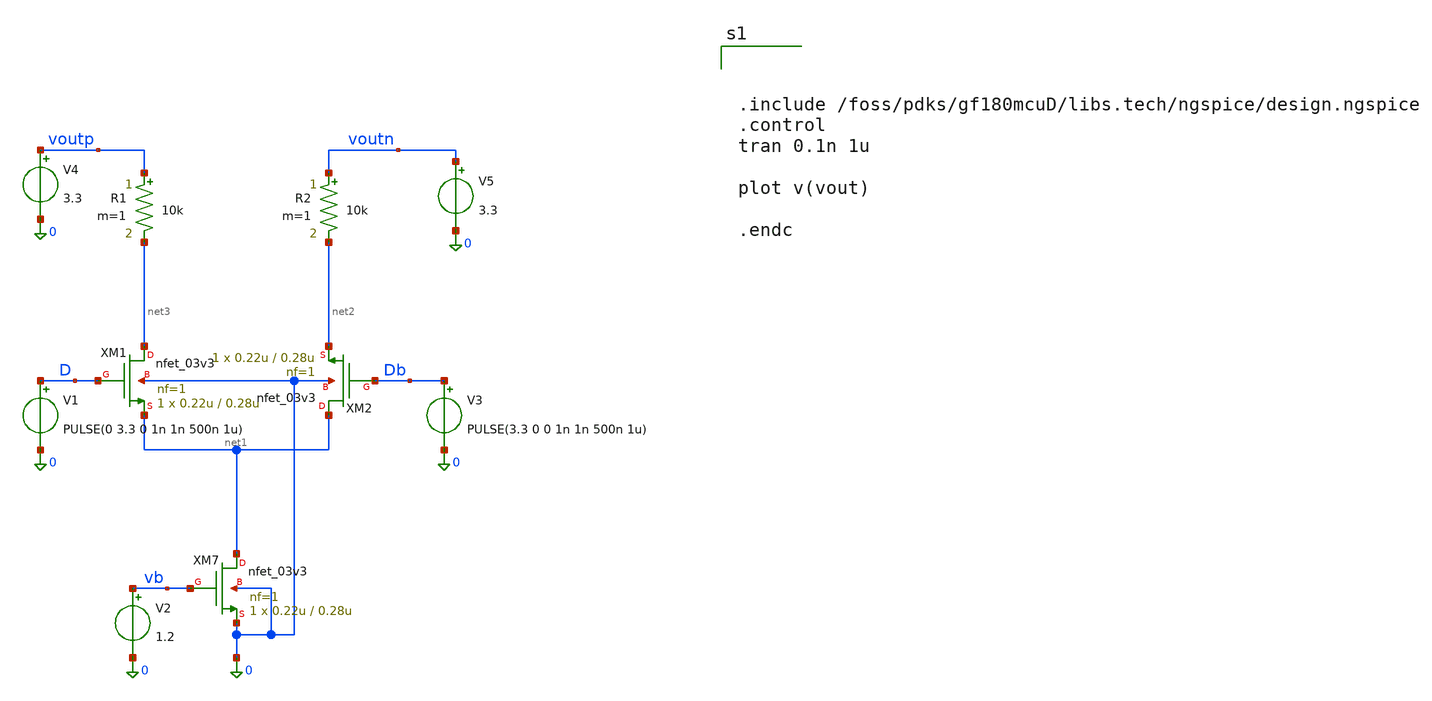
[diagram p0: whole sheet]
** sch_path: analog/dac/untitled-1.sch
**.subckt untitled-1
XM1 net3 D net1 0 nfet_03v3 L=0.28u W=0.22u nf=1 ad='int((nf+1)/2) * W/nf * 0.18u' as='int((nf+2)/2) * W/nf * 0.18u'
+ pd='2*int((nf+1)/2) * (W/nf + 0.18u)' ps='2*int((nf+2)/2) * (W/nf + 0.18u)' nrd='0.18u / W' nrs='0.18u / W'
+ sa=0 sb=0 sd=0 m=1
XM2 net1 Db net2 0 nfet_03v3 L=0.28u W=0.22u nf=1 ad='int((nf+1)/2) * W/nf * 0.18u' as='int((nf+2)/2) * W/nf * 0.18u'
+ pd='2*int((nf+1)/2) * (W/nf + 0.18u)' ps='2*int((nf+2)/2) * (W/nf + 0.18u)' nrd='0.18u / W' nrs='0.18u / W'
+ sa=0 sb=0 sd=0 m=1
XM7 net1 vb 0 0 nfet_03v3 L=0.28u W=0.22u nf=1 ad='int((nf+1)/2) * W/nf * 0.18u' as='int((nf+2)/2) * W/nf * 0.18u'
+ pd='2*int((nf+1)/2) * (W/nf + 0.18u)' ps='2*int((nf+2)/2) * (W/nf + 0.18u)' nrd='0.18u / W' nrs='0.18u / W'
+ sa=0 sb=0 sd=0 m=1
V1 D 0 PULSE(0 3.3 0 1n 1n 500n 1u)
V2 vb 0 1.2
V3 Db 0 PULSE(3.3 0 0 1n 1n 500n 1u)
R1 voutp net3 10k m=1
R2 voutn net2 10k m=1
V4 voutp 0 3.3
V5 voutn 0 3.3
**** begin user architecture code



.include /foss/pdks/gf180mcuD/libs.tech/ngspice/design.ngspice
.control
tran 0.1n 1u

plot v(vout)

.endc



**** end user architecture code
**.ends
.end
